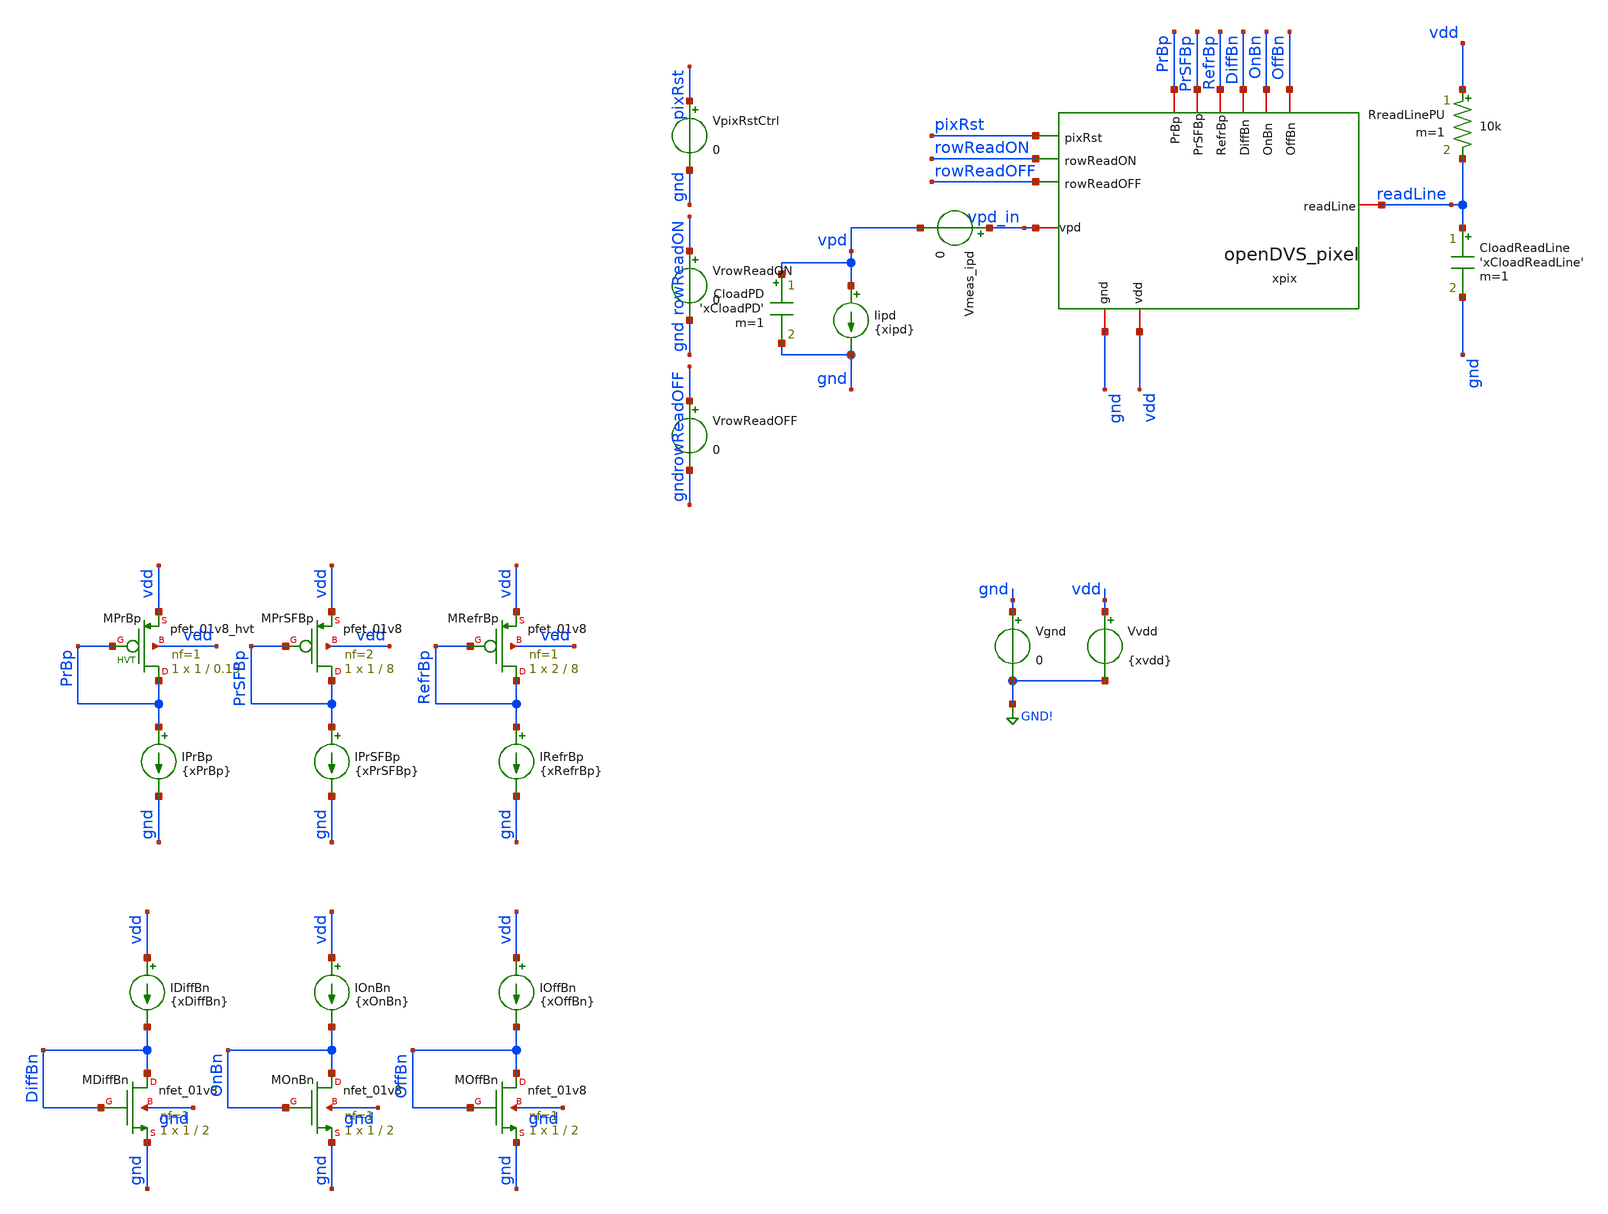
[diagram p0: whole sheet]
** sch_path: analog/xschem/tb_Pixel_autoreadLine_tran.sch
**.subckt tb_Pixel_autoreadLine_tran
xpix rowReadON vdd PrBp gnd vpd_in rowReadOFF pixRst PrSFBp DiffBn OnBn OffBn RefrBp readLine
+ openDVS_pixel
Vgnd gnd GND! 0
Vvdd vdd GND! {xvdd}
Iipd vpd gnd {xipd}
IRefrBp RefrBp gnd {xRefrBp}
XMRefrBp RefrBp RefrBp vdd vdd sky130_fd_pr__pfet_01v8 L=8 W=2 nf=1 ad='int((1 + 1)/2) * 2 / 1 * 0.29'
+ as='int((1 + 2)/2) * 2 / 1 * 0.29' pd='2*int((1 + 1)/2) * (2 / 1 + 0.29)' ps='2*int((1 + 2)/2) * (2 / 1 + 0.29)'
+ nrd='0.29 / 2 ' nrs='0.29 / 2 ' sa=0 sb=0 sd=0 mult=1 m=1
IPrBp PrBp gnd {xPrBp}
XMPrBp PrBp PrBp vdd vdd sky130_fd_pr__pfet_01v8_hvt L=0.15 W=1 nf=1 ad='int((1 + 1)/2) * 1 / 1 * 0.29'
+ as='int((1 + 2)/2) * 1 / 1 * 0.29' pd='2*int((1 + 1)/2) * (1 / 1 + 0.29)' ps='2*int((1 + 2)/2) * (1 / 1 + 0.29)'
+ nrd='0.29 / 1 ' nrs='0.29 / 1 ' sa=0 sb=0 sd=0 mult=1 m=1
IPrSFBp PrSFBp gnd {xPrSFBp}
XMDiffBn DiffBn DiffBn gnd gnd sky130_fd_pr__nfet_01v8 L=2 W=1 nf=1 ad='int((1 + 1)/2) * 1 / 1 * 0.29'
+ as='int((1 + 2)/2) * 1 / 1 * 0.29' pd='2*int((1 + 1)/2) * (1 / 1 + 0.29)' ps='2*int((1 + 2)/2) * (1 / 1 + 0.29)'
+ nrd='0.29 / 1 ' nrs='0.29 / 1 ' sa=0 sb=0 sd=0 mult=1 m=1
IDiffBn vdd DiffBn {xDiffBn}
XMOnBn OnBn OnBn gnd gnd sky130_fd_pr__nfet_01v8 L=2 W=1 nf=1 ad='int((1 + 1)/2) * 1 / 1 * 0.29' as='int((1 + 2)/2) * 1 / 1 * 0.29'
+ pd='2*int((1 + 1)/2) * (1 / 1 + 0.29)' ps='2*int((1 + 2)/2) * (1 / 1 + 0.29)' nrd='0.29 / 1 ' nrs='0.29 / 1 '
+ sa=0 sb=0 sd=0 mult=1 m=1
IOnBn vdd OnBn {xOnBn}
XMOffBn OffBn OffBn gnd gnd sky130_fd_pr__nfet_01v8 L=2 W=1 nf=1 ad='int((1 + 1)/2) * 1 / 1 * 0.29' as='int((1 + 2)/2) * 1 / 1 * 0.29'
+ pd='2*int((1 + 1)/2) * (1 / 1 + 0.29)' ps='2*int((1 + 2)/2) * (1 / 1 + 0.29)' nrd='0.29 / 1 ' nrs='0.29 / 1 '
+ sa=0 sb=0 sd=0 mult=1 m=1
IOffBn vdd OffBn {xOffBn}
CloadReadLine readLine gnd 'xCloadReadLine' m=1
CloadPD vpd gnd 'xCloadPD' m=1
Vmeas_ipd vpd_in vpd 0
XMPrSFBp PrSFBp PrSFBp vdd vdd sky130_fd_pr__pfet_01v8 L=8 W=1 nf=2 ad='int((2 + 1)/2) * 1 / 2 * 0.29'
+ as='int((2 + 2)/2) * 1 / 2 * 0.29' pd='2*int((2 + 1)/2) * (1 / 2 + 0.29)' ps='2*int((2 + 2)/2) * (1 / 2 + 0.29)'
+ nrd='0.29 / 1 ' nrs='0.29 / 1 ' sa=0 sb=0 sd=0 mult=1 m=1
RreadLinePU vdd readLine 10k m=1
VpixRstCtrl pixRst gnd 0
VrowReadON rowReadON gnd 0
VrowReadOFF rowReadOFF gnd 0
**** begin user architecture code

** opencircuitdesign pdks install
.lib $::SKYWATER_MODELS/sky130.lib.spice tt



** Convergence options for nA-range weak-inversion pixel circuit
.option gmin=1e-16 abstol=1e-15 vntol=1e-9 reltol=1e-4 chgtol=1e-16
.option method=gear maxord=2 trtol=1
.option itl1=500 itl2=200 itl4=50
.option gminsteps=200 srcsteps=200
.option ramptime=100n

.param xvdd = 1.8
.param xipd = 1e-9
.param xPrBp = 10n
.param xPrSFBp = 100p
.param xRefrBp = 4n
.param xDiffBn = 10n
.param xOnBn = 100n
.param xOffBn = 1n

.param xCloadPD = 30f
.param xCloadReadLine = 300f

*Small Iphoto testing
Iphoto1 vpd gnd pulse(50n 100n 120m 50m 50m 59.9m 300m)
Iphoto2 vpd gnd pulse(50n 25n 240m 50m 50m 59.9m 300m)

.save all
.save v(xpix.on) v(xpix.noff)

.control

** ============================================================
** Event-driven auto-read testbench
** Detects xpix.ON rising or xpix.nOFF falling, then generates
** the read sequence: rowReadON, rowReadOFF, rowReadON (reset)
** ============================================================

** Read sequence timing (parameterizable)
let xevent_delay = 1e-6
let xread_on_len = 950e-9
let xgap = 50e-9
let xread_off_len = 950e-9
let xrst_phase_len = 950e-9
let xsettle = 100e-6

let sim_end = 0.39
let tran_end = sim_end + 1

** Phase 0: let circuit initialize (10ms settling)
** tran end time must exceed sim_end to avoid resume-after-finished crash
stop when time > 10e-3
tran 1u $&tran_end uic
let vdd_val = v(vdd)[length(v(vdd))-1]
let on_thresh = 0.9 * vdd_val
let noff_thresh = 0.1 * vdd_val

echo
echo '=== Auto-read TB initialized ==='
echo '    VDD =' $&vdd_val 'V'
echo '    ON thresh =' $&on_thresh 'V'
echo '    nOFF thresh =' $&noff_thresh 'V'

** Event-driven readout loop (runs until sim_end)
let event_count = 0
let t_now = time[length(time)-1]

while t_now < $&sim_end - 1e-9
  ** Arm event breakpoints
  delete all
  stop when v(xpix.on) > $&on_thresh
  stop when v(xpix.noff) < $&noff_thresh
  stop when time > $&sim_end
  resume

  let t_now = time[length(time)-1]
  if t_now >= $&sim_end - 1e-9
    break
  end

  let event_count = event_count + 1
  let t_event = t_now
  echo
  echo '=== Event #' $&event_count 'at t =' $&t_event 's ==='

  ** Skip read sequence if not enough time left
  let t_seq_end = t_event + xevent_delay + xread_on_len + xgap + xread_off_len + xgap +
+ xrst_phase_len + xsettle
  if t_seq_end > $&sim_end
    echo '    Skipping read sequence - too close to sim_end'
    break
  end

  ** Wait parameterized delay before read sequence
  delete all
  let t1 = t_event + xevent_delay
  stop when time > $&t1
  resume

  ** Phase 1: rowReadON (read ON phase)
  alter vrowreadon = $&vdd_val
  delete all
  let t2 = t1 + xread_on_len
  stop when time > $&t2
  resume
  alter vrowreadon = 0

  ** Gap
  delete all
  let t3 = t2 + xgap
  stop when time > $&t3
  resume

  ** Phase 2: rowReadOFF
  alter vrowreadoff = $&vdd_val
  delete all
  let t4 = t3 + xread_off_len
  stop when time > $&t4
  resume
  alter vrowreadoff = 0

  ** Gap
  delete all
  let t5 = t4 + xgap
  stop when time > $&t5
  resume

  ** Phase 3: rowReadON (reset phase) + pixRst
  alter vrowreadon = $&vdd_val
  alter vpixrstctrl = $&vdd_val
  delete all
  let t6 = t5 + xrst_phase_len
  stop when time > $&t6
  resume
  alter vrowreadon = 0
  alter vpixrstctrl = 0

  ** Post-reset settle before re-arming event detection
  delete all
  let t7 = t6 + xsettle
  stop when time > $&t7
  resume
  let t_now = time[length(time)-1]
end

** Run to sim_end to ensure complete waveform
delete all
stop when time > $&sim_end
resume

echo
echo '=== Simulation complete:' $&event_count 'events detected ==='
setplot tran1
write tb_Pixel_autoreadLine_tran.raw
.endc


**** end user architecture code
**.ends

* expanding   symbol:  openDVS_pixel.sym # of pins=13
** sym_path: analog/xschem/openDVS_pixel.sym
** sch_path: analog/xschem/openDVS_pixel.sch
.subckt openDVS_pixel rowReadON vdd PrBp gnd vpd rowReadOFF pixRst PrSFBp DiffBn OnBn OffBn RefrBp
+ readLine
*.iopin vpd
*.iopin PrBp
*.iopin gnd
*.iopin vdd
*.iopin PrSFBp
*.iopin DiffBn
*.iopin OnBn
*.iopin OffBn
*.iopin RefrBp
*.ipin pixRst
*.ipin rowReadON
*.ipin rowReadOFF
*.iopin readLine
xpr vdd PrBp gnd vpd vpr PixelPhotoreceptor
xsf vdd PrSFBp gnd vpr vsf PixelSourceFollower
xsf1 vdd DiffBn gnd vsf vdiff nRst PixelChangeAmplifier
xcomp vdd OnBn gnd vdiff ON OffBn nOFF PixelComparators
xhandshake rowReadOFF gnd rowReadON readLine nOFF ON PixelHandshake
xrst rowReadON gnd pixRst nRst RefrBp vdd PixelResetGen
.ends


* expanding   symbol:  PixelPhotoreceptor.sym # of pins=5
** sym_path: analog/xschem/PixelPhotoreceptor.sym
** sch_path: analog/xschem/PixelPhotoreceptor.sch
.subckt PixelPhotoreceptor vdd PrBp gnd vpd vpr
*.iopin PrBp
*.iopin vdd
*.iopin vpd
*.iopin gnd
*.iopin vpr
XMpd vdd vpr vpd gnd sky130_fd_pr__nfet_01v8 L=0.3 W=0.5 nf=1 ad='int((1 + 1)/2) * 0.5 / 1 * 0.29' as='int((1 + 2)/2) * 0.5 / 1 * 0.29'
+ pd='2*int((1 + 1)/2) * (0.5 / 1 + 0.29)' ps='2*int((1 + 2)/2) * (0.5 / 1 + 0.29)' nrd='0.29 / 0.5 ' nrs='0.29 / 0.5 '
+ sa=0 sb=0 sd=0 mult=1 m=1
XMpr_amp vpr vpd gnd gnd sky130_fd_pr__nfet_01v8 L=0.3 W=0.5 nf=1 ad='int((1 + 1)/2) * 0.5 / 1 * 0.29'
+ as='int((1 + 2)/2) * 0.5 / 1 * 0.29' pd='2*int((1 + 1)/2) * (0.5 / 1 + 0.29)' ps='2*int((1 + 2)/2) * (0.5 / 1 + 0.29)'
+ nrd='0.29 / 0.5 ' nrs='0.29 / 0.5 ' sa=0 sb=0 sd=0 mult=1 m=1
XMprBias vpr PrBp vdd vdd sky130_fd_pr__pfet_01v8_hvt L=0.3 W=1 nf=1 ad='int((1 + 1)/2) * 1 / 1 * 0.29'
+ as='int((1 + 2)/2) * 1 / 1 * 0.29' pd='2*int((1 + 1)/2) * (1 / 1 + 0.29)' ps='2*int((1 + 2)/2) * (1 / 1 + 0.29)'
+ nrd='0.29 / 1 ' nrs='0.29 / 1 ' sa=0 sb=0 sd=0 mult=1 m=1
.ends


* expanding   symbol:  PixelSourceFollower.sym # of pins=5
** sym_path: analog/xschem/PixelSourceFollower.sym
** sch_path: analog/xschem/PixelSourceFollower.sch
.subckt PixelSourceFollower vdd PrSFBp gnd vpr vsf
*.iopin gnd
*.iopin PrSFBp
*.iopin vpr
*.iopin vsf
*.iopin vdd
XMsfBias vsf PrSFBp vdd vdd sky130_fd_pr__pfet_01v8 L=4 W=1 nf=1 ad='int((1 + 1)/2) * 1 / 1 * 0.29' as='int((1 + 2)/2) * 1 / 1 * 0.29'
+ pd='2*int((1 + 1)/2) * (1 / 1 + 0.29)' ps='2*int((1 + 2)/2) * (1 / 1 + 0.29)' nrd='0.29 / 1 ' nrs='0.29 / 1 '
+ sa=0 sb=0 sd=0 mult=1 m=1
XMsf1 gnd vpr vsf vdd sky130_fd_pr__pfet_01v8 L=1 W=2 nf=1 ad='int((1 + 1)/2) * 2 / 1 * 0.29' as='int((1 + 2)/2) * 2 / 1 * 0.29'
+ pd='2*int((1 + 1)/2) * (2 / 1 + 0.29)' ps='2*int((1 + 2)/2) * (2 / 1 + 0.29)' nrd='0.29 / 2 ' nrs='0.29 / 2 '
+ sa=0 sb=0 sd=0 mult=1 m=1
.ends


* expanding   symbol:  PixelChangeAmplifier.sym # of pins=6
** sym_path: analog/xschem/PixelChangeAmplifier.sym
** sch_path: analog/xschem/PixelChangeAmplifier.sch
.subckt PixelChangeAmplifier vdd DiffBn gnd vsf vdiff nRst
*.iopin DiffBn
*.iopin vsf
*.iopin vdd
*.iopin gnd
*.iopin vdiff
*.iopin nRst
XC1 vsf vd sky130_fd_pr__cap_mim_m3_1 W=1 L=1 MF=40 m=40
XC2 vd vdiff sky130_fd_pr__cap_mim_m3_1 W=1 L=1 MF=2 m=2
XMchAmpBias vdiff DiffBn gnd gnd sky130_fd_pr__nfet_01v8 L=2 W=2 nf=1 ad='int((1 + 1)/2) * 2 / 1 * 0.29'
+ as='int((1 + 2)/2) * 2 / 1 * 0.29' pd='2*int((1 + 1)/2) * (2 / 1 + 0.29)' ps='2*int((1 + 2)/2) * (2 / 1 + 0.29)'
+ nrd='0.29 / 2 ' nrs='0.29 / 2 ' sa=0 sb=0 sd=0 mult=1 m=1
XMrst vdiff nRst vd vdd sky130_fd_pr__pfet_01v8_hvt L=0.3 W=1 nf=1 ad='int((1 + 1)/2) * 1 / 1 * 0.29'
+ as='int((1 + 2)/2) * 1 / 1 * 0.29' pd='2*int((1 + 1)/2) * (1 / 1 + 0.29)' ps='2*int((1 + 2)/2) * (1 / 1 + 0.29)'
+ nrd='0.29 / 1 ' nrs='0.29 / 1 ' sa=0 sb=0 sd=0 mult=1 m=1
XMchAmp vdiff vd vdd vdd sky130_fd_pr__pfet_01v8_hvt L=2 W=2 nf=1 ad='int((1 + 1)/2) * 2 / 1 * 0.29'
+ as='int((1 + 2)/2) * 2 / 1 * 0.29' pd='2*int((1 + 1)/2) * (2 / 1 + 0.29)' ps='2*int((1 + 2)/2) * (2 / 1 + 0.29)'
+ nrd='0.29 / 2 ' nrs='0.29 / 2 ' sa=0 sb=0 sd=0 mult=1 m=1
.ends


* expanding   symbol:  PixelComparators.sym # of pins=7
** sym_path: analog/xschem/PixelComparators.sym
** sch_path: analog/xschem/PixelComparators.sch
.subckt PixelComparators vdd OnBn gnd vdiff ON OffBn nOFF
*.iopin OnBn
*.iopin OffBn
*.iopin vdd
*.iopin vdiff
*.iopin gnd
*.iopin ON
*.iopin nOFF
XMonBias ON OnBn gnd gnd sky130_fd_pr__nfet_01v8 L=2 W=2 nf=1 ad='int((1 + 1)/2) * 2 / 1 * 0.29' as='int((1 + 2)/2) * 2 / 1 * 0.29'
+ pd='2*int((1 + 1)/2) * (2 / 1 + 0.29)' ps='2*int((1 + 2)/2) * (2 / 1 + 0.29)' nrd='0.29 / 2 ' nrs='0.29 / 2 '
+ sa=0 sb=0 sd=0 mult=1 m=1
XMoffBias nOFF OffBn gnd gnd sky130_fd_pr__nfet_01v8 L=2 W=2 nf=1 ad='int((1 + 1)/2) * 2 / 1 * 0.29'
+ as='int((1 + 2)/2) * 2 / 1 * 0.29' pd='2*int((1 + 1)/2) * (2 / 1 + 0.29)' ps='2*int((1 + 2)/2) * (2 / 1 + 0.29)'
+ nrd='0.29 / 2 ' nrs='0.29 / 2 ' sa=0 sb=0 sd=0 mult=1 m=1
XMon ON vdiff vdd vdd sky130_fd_pr__pfet_01v8_hvt L=2 W=2 nf=1 ad='int((1 + 1)/2) * 2 / 1 * 0.29' as='int((1 + 2)/2) * 2 / 1 * 0.29'
+ pd='2*int((1 + 1)/2) * (2 / 1 + 0.29)' ps='2*int((1 + 2)/2) * (2 / 1 + 0.29)' nrd='0.29 / 2 ' nrs='0.29 / 2 '
+ sa=0 sb=0 sd=0 mult=1 m=1
XMoff nOFF vdiff vdd vdd sky130_fd_pr__pfet_01v8_hvt L=2 W=2 nf=1 ad='int((1 + 1)/2) * 2 / 1 * 0.29'
+ as='int((1 + 2)/2) * 2 / 1 * 0.29' pd='2*int((1 + 1)/2) * (2 / 1 + 0.29)' ps='2*int((1 + 2)/2) * (2 / 1 + 0.29)'
+ nrd='0.29 / 2 ' nrs='0.29 / 2 ' sa=0 sb=0 sd=0 mult=1 m=1
.ends


* expanding   symbol:  PixelHandshake.sym # of pins=6
** sym_path: analog/xschem/PixelHandshake.sym
** sch_path: analog/xschem/PixelHandshake.sch
.subckt PixelHandshake rowReadOFF gnd rowReadON readLine ON nOFF
*.ipin rowReadON
*.ipin rowReadOFF
*.iopin readLine
*.iopin ON
*.iopin nOFF
*.iopin gnd
XMswON readLine rowReadON readLineONpd gnd sky130_fd_pr__nfet_01v8 L=0.15 W=0.5 nf=1 ad='int((1 + 1)/2) * 0.5 / 1 * 0.29'
+ as='int((1 + 2)/2) * 0.5 / 1 * 0.29' pd='2*int((1 + 1)/2) * (0.5 / 1 + 0.29)' ps='2*int((1 + 2)/2) * (0.5 / 1 + 0.29)'
+ nrd='0.29 / 0.5 ' nrs='0.29 / 0.5 ' sa=0 sb=0 sd=0 mult=1 m=1
XMoutON readLineONpd ON gnd gnd sky130_fd_pr__nfet_01v8 L=0.15 W=0.5 nf=1 ad='int((1 + 1)/2) * 0.5 / 1 * 0.29'
+ as='int((1 + 2)/2) * 0.5 / 1 * 0.29' pd='2*int((1 + 1)/2) * (0.5 / 1 + 0.29)' ps='2*int((1 + 2)/2) * (0.5 / 1 + 0.29)'
+ nrd='0.29 / 0.5 ' nrs='0.29 / 0.5 ' sa=0 sb=0 sd=0 mult=1 m=1
XMswOFF readLine rowReadOFF readLineOFFpd gnd sky130_fd_pr__nfet_01v8 L=0.15 W=0.5 nf=1 ad='int((1 + 1)/2) * 0.5 / 1 * 0.29'
+ as='int((1 + 2)/2) * 0.5 / 1 * 0.29' pd='2*int((1 + 1)/2) * (0.5 / 1 + 0.29)' ps='2*int((1 + 2)/2) * (0.5 / 1 + 0.29)'
+ nrd='0.29 / 0.5 ' nrs='0.29 / 0.5 ' sa=0 sb=0 sd=0 mult=1 m=1
XMoutOFF readLineOFFpd nOFF gnd gnd sky130_fd_pr__nfet_01v8 L=0.15 W=0.5 nf=1 ad='int((1 + 1)/2) * 0.5 / 1 * 0.29'
+ as='int((1 + 2)/2) * 0.5 / 1 * 0.29' pd='2*int((1 + 1)/2) * (0.5 / 1 + 0.29)' ps='2*int((1 + 2)/2) * (0.5 / 1 + 0.29)'
+ nrd='0.29 / 0.5 ' nrs='0.29 / 0.5 ' sa=0 sb=0 sd=0 mult=1 m=1
.ends


* expanding   symbol:  PixelResetGen.sym # of pins=6
** sym_path: analog/xschem/PixelResetGen.sym
** sch_path: analog/xschem/PixelResetGen.sch
.subckt PixelResetGen rowRst gnd colRst nRst RefrBp vdd
*.ipin rowRst
*.ipin colRst
*.iopin RefrBp
*.iopin gnd
*.iopin vdd
*.iopin nRst
XMrefrInv nRst colRst net1 gnd sky130_fd_pr__nfet_01v8 L=0.15 W=0.5 nf=1 ad='int((1 + 1)/2) * 0.5 / 1 * 0.29'
+ as='int((1 + 2)/2) * 0.5 / 1 * 0.29' pd='2*int((1 + 1)/2) * (0.5 / 1 + 0.29)' ps='2*int((1 + 2)/2) * (0.5 / 1 + 0.29)'
+ nrd='0.29 / 0.5 ' nrs='0.29 / 0.5 ' sa=0 sb=0 sd=0 mult=1 m=1
XMrefrBias nRst RefrBp vdd vdd sky130_fd_pr__pfet_01v8 L=8 W=2 nf=1 ad='int((1 + 1)/2) * 2 / 1 * 0.29'
+ as='int((1 + 2)/2) * 2 / 1 * 0.29' pd='2*int((1 + 1)/2) * (2 / 1 + 0.29)' ps='2*int((1 + 2)/2) * (2 / 1 + 0.29)'
+ nrd='0.29 / 2 ' nrs='0.29 / 2 ' sa=0 sb=0 sd=0 mult=1 m=1
XMcapRefr vdd nRst vdd vdd sky130_fd_pr__pfet_01v8_hvt L=8 W=8 nf=1 ad='int((1 + 1)/2) * 8 / 1 * 0.29'
+ as='int((1 + 2)/2) * 8 / 1 * 0.29' pd='2*int((1 + 1)/2) * (8 / 1 + 0.29)' ps='2*int((1 + 2)/2) * (8 / 1 + 0.29)'
+ nrd='0.29 / 8 ' nrs='0.29 / 8 ' sa=0 sb=0 sd=0 mult=1 m=1
XMswON1 net1 rowRst gnd gnd sky130_fd_pr__nfet_01v8 L=0.15 W=0.5 nf=1 ad='int((1 + 1)/2) * 0.5 / 1 * 0.29'
+ as='int((1 + 2)/2) * 0.5 / 1 * 0.29' pd='2*int((1 + 1)/2) * (0.5 / 1 + 0.29)' ps='2*int((1 + 2)/2) * (0.5 / 1 + 0.29)'
+ nrd='0.29 / 0.5 ' nrs='0.29 / 0.5 ' sa=0 sb=0 sd=0 mult=1 m=1
.ends

.GLOBAL GND!
.end
